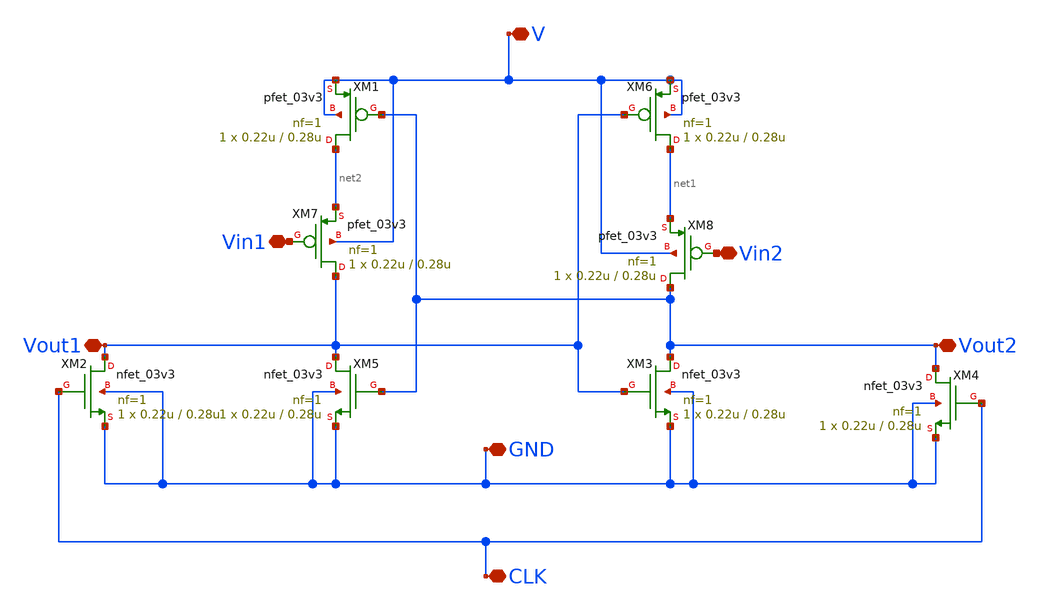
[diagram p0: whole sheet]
** sch_path: V2/Symbols/strongarm.sch
**.subckt strongarm V Vout1 Vin1 Vin2 Vout2 CLK GND
*.iopin V
*.iopin Vout1
*.iopin Vin1
*.iopin Vin2
*.iopin Vout2
*.iopin CLK
*.iopin GND
XM1 net2 Vout2 V V pfet_03v3 L=0.28u W=0.22u nf=1 ad='int((nf+1)/2) * W/nf * 0.18u' as='int((nf+2)/2) * W/nf * 0.18u'
+ pd='2*int((nf+1)/2) * (W/nf + 0.18u)' ps='2*int((nf+2)/2) * (W/nf + 0.18u)' nrd='0.18u / W' nrs='0.18u / W'
+ sa=0 sb=0 sd=0 m=1
XM2 Vout1 CLK GND GND nfet_03v3 L=0.28u W=0.22u nf=1 ad='int((nf+1)/2) * W/nf * 0.18u' as='int((nf+2)/2) * W/nf * 0.18u'
+ pd='2*int((nf+1)/2) * (W/nf + 0.18u)' ps='2*int((nf+2)/2) * (W/nf + 0.18u)' nrd='0.18u / W' nrs='0.18u / W'
+ sa=0 sb=0 sd=0 m=1
XM3 Vout2 Vout1 GND GND nfet_03v3 L=0.28u W=0.22u nf=1 ad='int((nf+1)/2) * W/nf * 0.18u' as='int((nf+2)/2) * W/nf * 0.18u'
+ pd='2*int((nf+1)/2) * (W/nf + 0.18u)' ps='2*int((nf+2)/2) * (W/nf + 0.18u)' nrd='0.18u / W' nrs='0.18u / W'
+ sa=0 sb=0 sd=0 m=1
XM4 Vout2 CLK GND GND nfet_03v3 L=0.28u W=0.22u nf=1 ad='int((nf+1)/2) * W/nf * 0.18u' as='int((nf+2)/2) * W/nf * 0.18u'
+ pd='2*int((nf+1)/2) * (W/nf + 0.18u)' ps='2*int((nf+2)/2) * (W/nf + 0.18u)' nrd='0.18u / W' nrs='0.18u / W'
+ sa=0 sb=0 sd=0 m=1
XM5 Vout1 Vout2 GND GND nfet_03v3 L=0.28u W=0.22u nf=1 ad='int((nf+1)/2) * W/nf * 0.18u' as='int((nf+2)/2) * W/nf * 0.18u'
+ pd='2*int((nf+1)/2) * (W/nf + 0.18u)' ps='2*int((nf+2)/2) * (W/nf + 0.18u)' nrd='0.18u / W' nrs='0.18u / W'
+ sa=0 sb=0 sd=0 m=1
XM6 net1 Vout1 V V pfet_03v3 L=0.28u W=0.22u nf=1 ad='int((nf+1)/2) * W/nf * 0.18u' as='int((nf+2)/2) * W/nf * 0.18u'
+ pd='2*int((nf+1)/2) * (W/nf + 0.18u)' ps='2*int((nf+2)/2) * (W/nf + 0.18u)' nrd='0.18u / W' nrs='0.18u / W'
+ sa=0 sb=0 sd=0 m=1
XM7 Vout1 Vin1 net2 V pfet_03v3 L=0.28u W=0.22u nf=1 ad='int((nf+1)/2) * W/nf * 0.18u' as='int((nf+2)/2) * W/nf * 0.18u'
+ pd='2*int((nf+1)/2) * (W/nf + 0.18u)' ps='2*int((nf+2)/2) * (W/nf + 0.18u)' nrd='0.18u / W' nrs='0.18u / W'
+ sa=0 sb=0 sd=0 m=1
XM8 Vout2 Vin2 net1 V pfet_03v3 L=0.28u W=0.22u nf=1 ad='int((nf+1)/2) * W/nf * 0.18u' as='int((nf+2)/2) * W/nf * 0.18u'
+ pd='2*int((nf+1)/2) * (W/nf + 0.18u)' ps='2*int((nf+2)/2) * (W/nf + 0.18u)' nrd='0.18u / W' nrs='0.18u / W'
+ sa=0 sb=0 sd=0 m=1
**** begin user architecture code

.include /foss/pdks/gf180mcuC/libs.tech/ngspice/design.ngspice
.lib /foss/pdks/gf180mcuC/libs.tech/ngspice/sm141064.ngspice typical

**** end user architecture code
**.ends
.end
